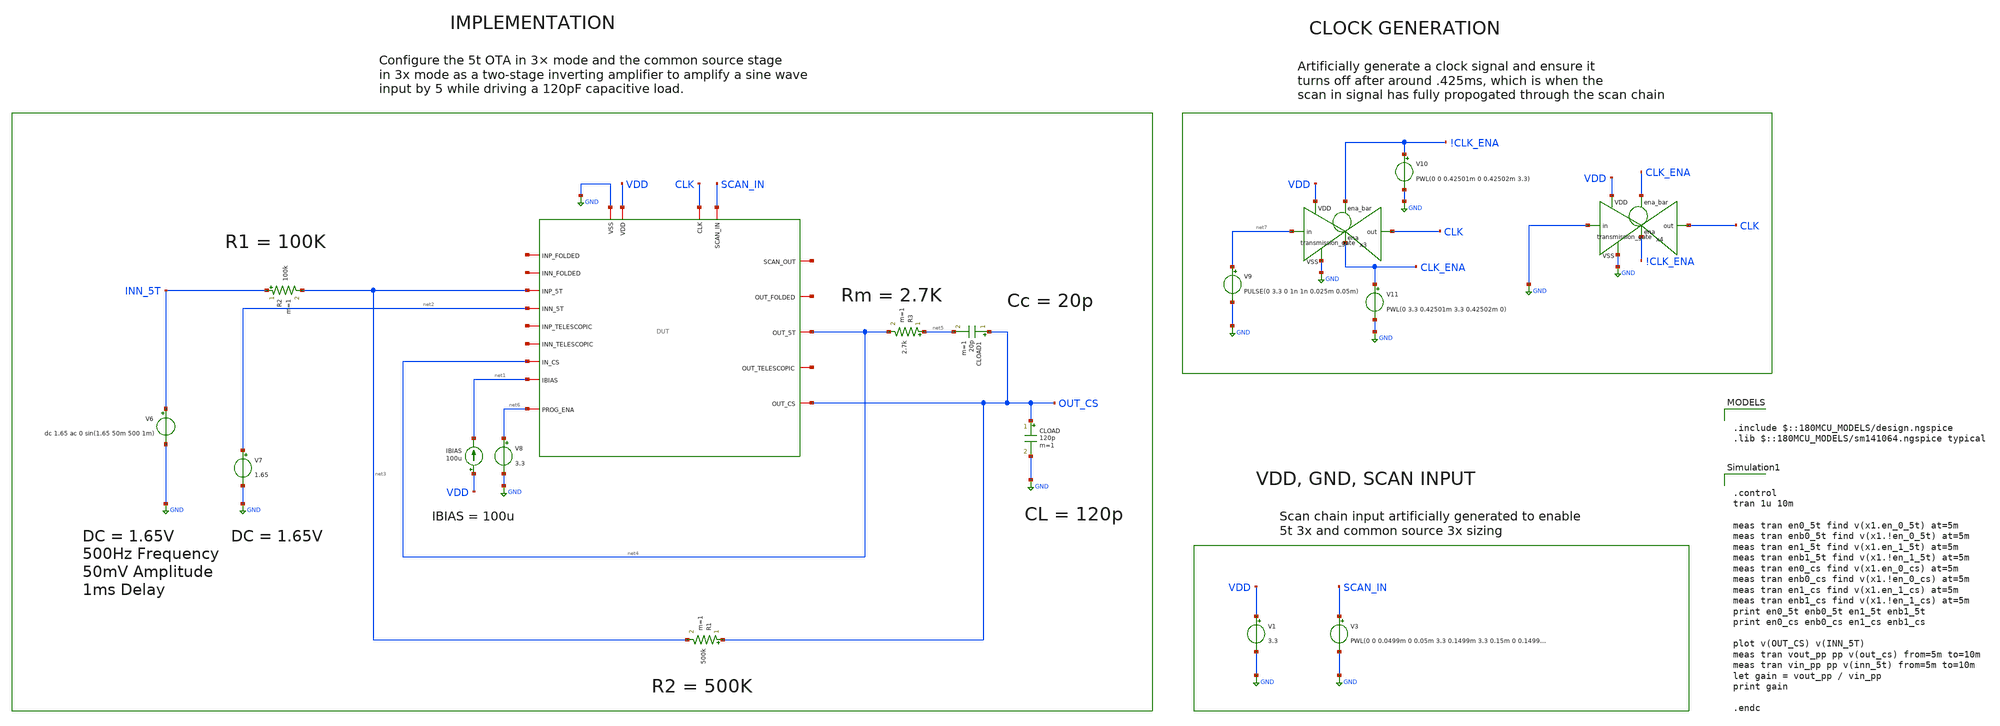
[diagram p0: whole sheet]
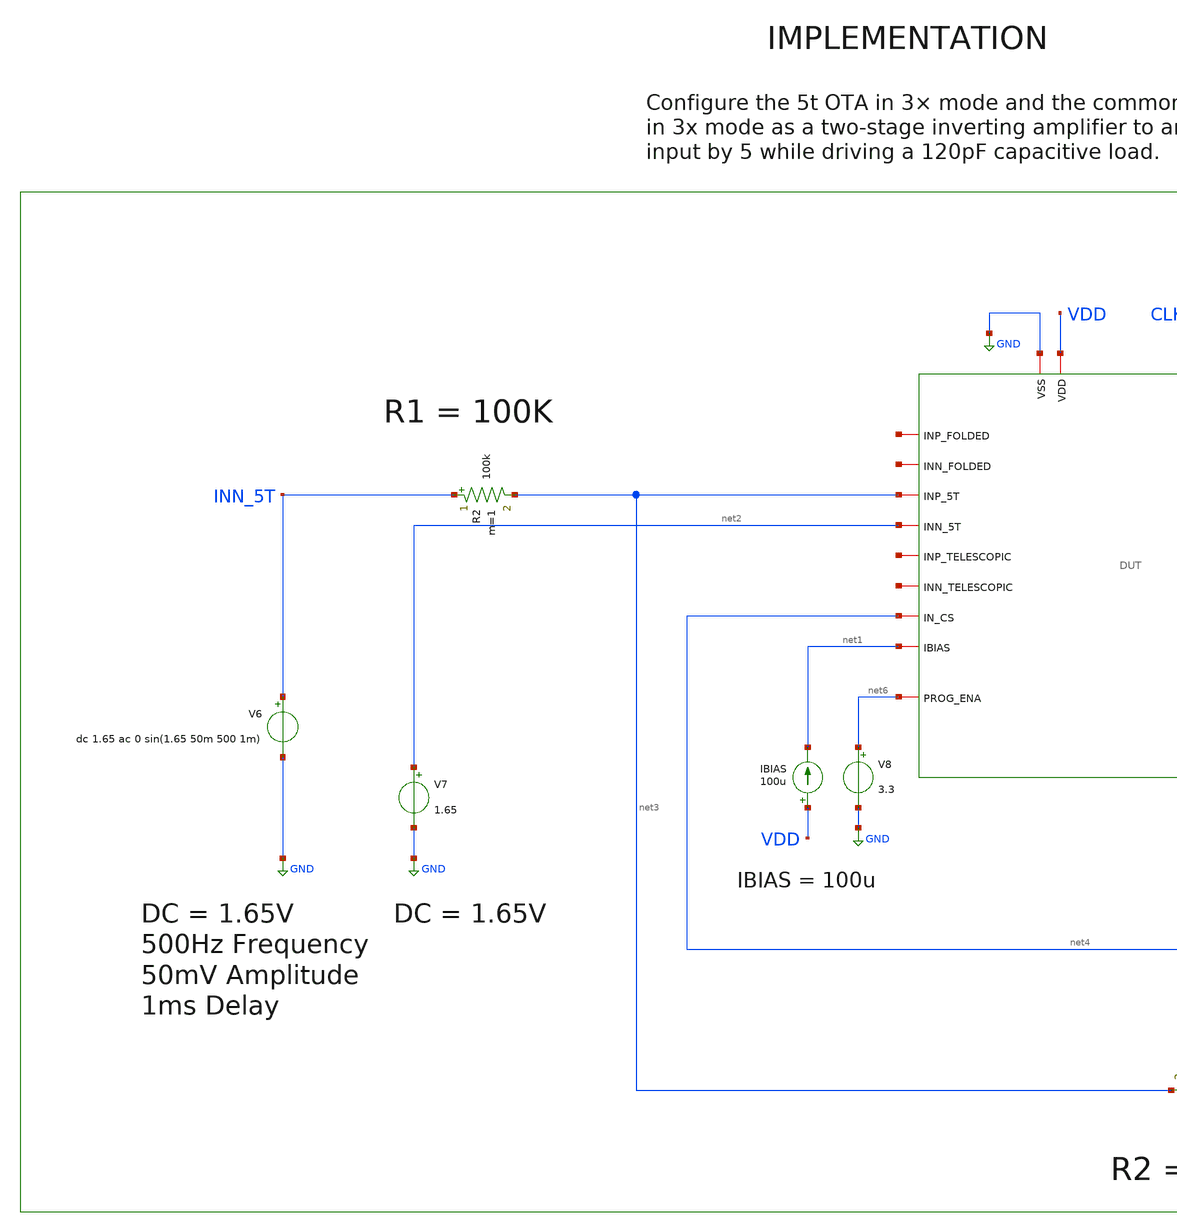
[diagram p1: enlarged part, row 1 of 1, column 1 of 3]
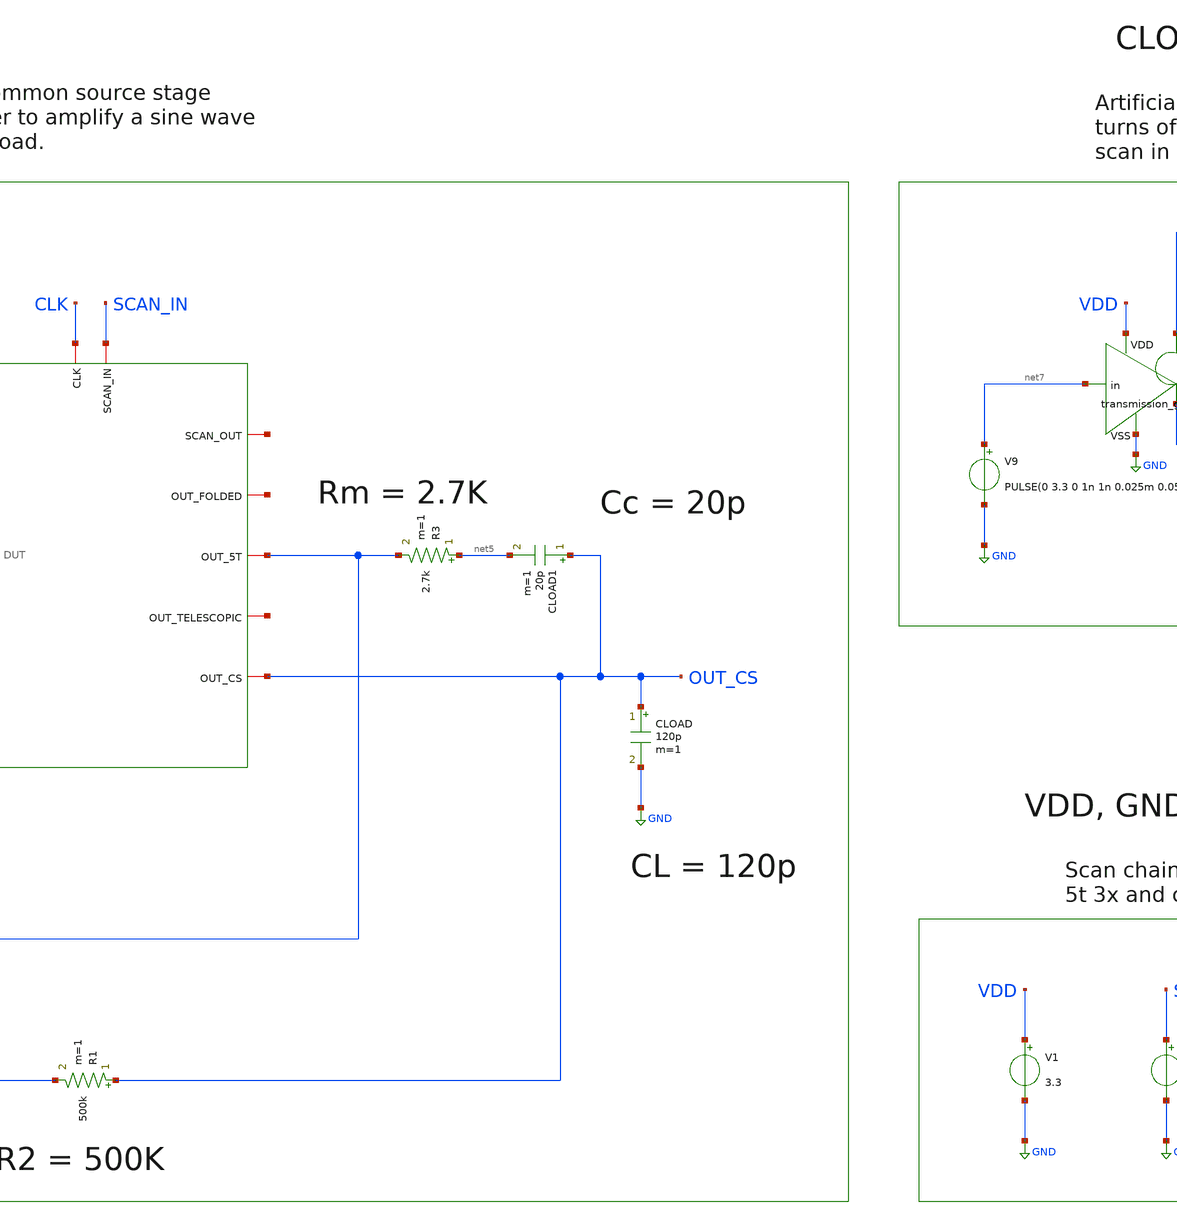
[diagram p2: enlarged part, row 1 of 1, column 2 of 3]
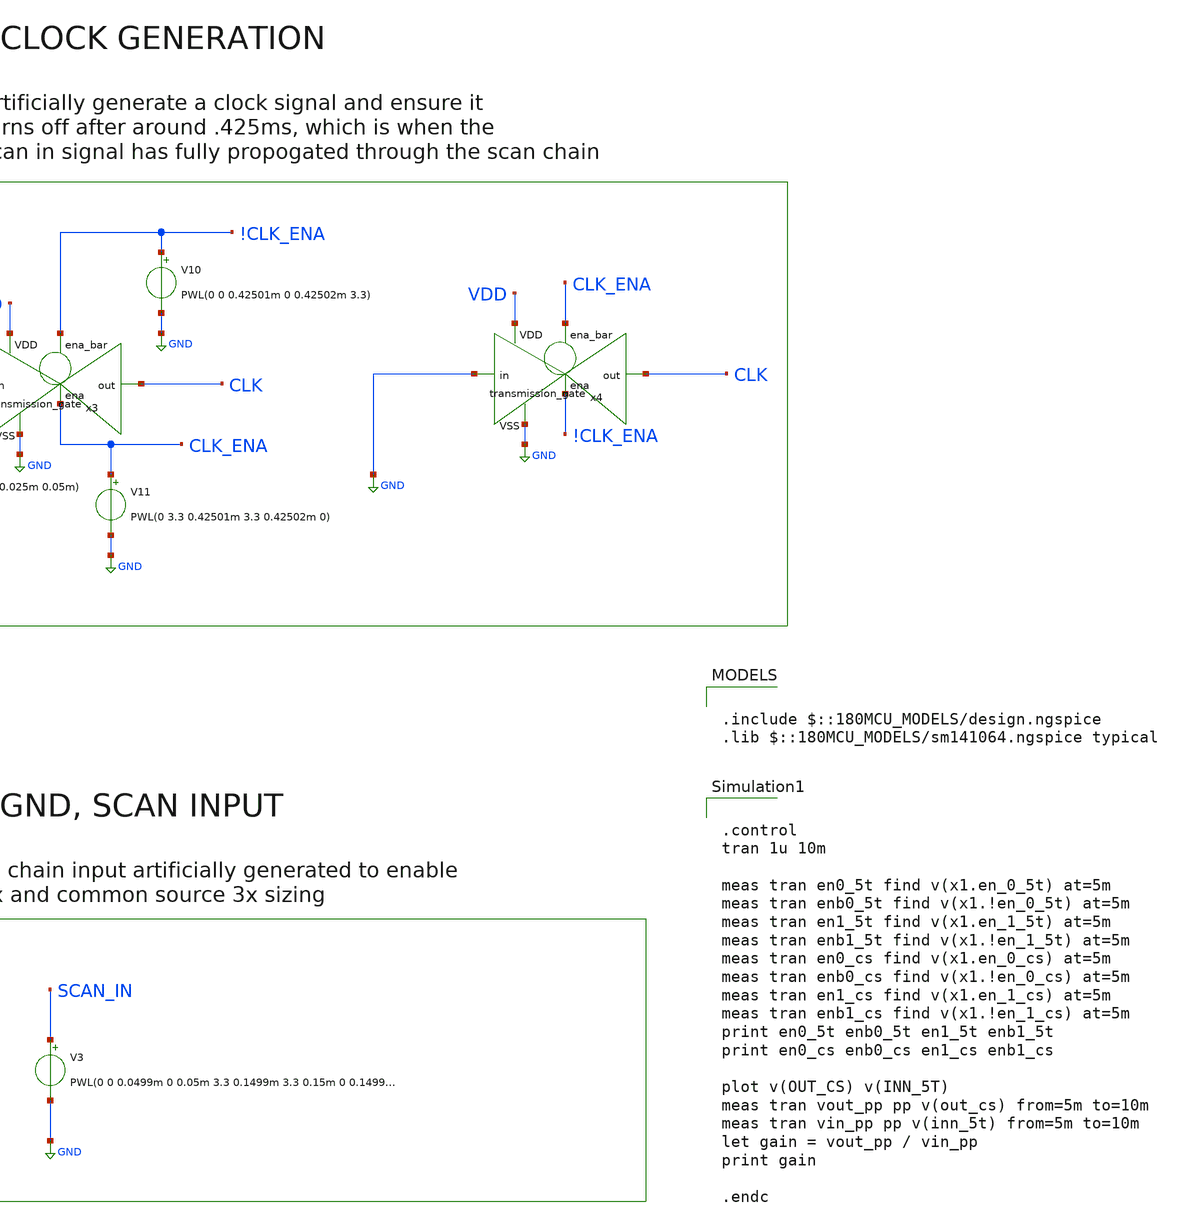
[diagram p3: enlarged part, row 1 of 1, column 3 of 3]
** sch_path: designs/libs/core_tb/sl/ota_5t/two_stage/5t_inverting_cs.sch
**.subckt 5t_inverting_cs
V3 SCAN_IN GND PWL(0 0 0.0499m 0 0.05m 3.3 0.1499m 3.3 0.15m 0 0.1499m 0 0.15m 3.3 0.24999m 3.3
+ 0.25m 0)
V1 VDD GND 3.3
IBIAS VDD net1 100u
CLOAD OUT_CS GND 120p m=1
R3 net5 net4 2.7k m=1
CLOAD1 OUT_CS net5 20p m=1
V7 net2 GND 1.65
R2 INN_5T net3 100k m=1
R1 OUT_CS net3 500k m=1
V6 INN_5T GND dc 1.65 ac 0 sin(1.65 50m 500 1m)
x1 CLK net8 SCAN_IN GND VDD net9 net10 net4 net1 net11 net3 net2 net12 net13 OUT_CS net4 net14 net6
+ DUT
V8 net6 GND 3.3
V9 net7 GND PULSE(0 3.3 0 1n 1n 0.025m 0.05m)
x3 !CLK_ENA VDD CLK net7 GND CLK_ENA transmission_gate
V10 !CLK_ENA GND PWL(0 0 0.42501m 0 0.42502m 3.3)
V11 CLK_ENA GND PWL(0 3.3 0.42501m 3.3 0.42502m 0)
x4 CLK_ENA VDD CLK GND GND !CLK_ENA transmission_gate
**** begin user architecture code

.include $::180MCU_MODELS/design.ngspice
.lib $::180MCU_MODELS/sm141064.ngspice typical



.control
tran 1u 10m

meas tran en0_5t find v(x1.en_0_5t) at=5m
meas tran enb0_5t find v(x1.!en_0_5t) at=5m
meas tran en1_5t find v(x1.en_1_5t) at=5m
meas tran enb1_5t find v(x1.!en_1_5t) at=5m
meas tran en0_cs find v(x1.en_0_cs) at=5m
meas tran enb0_cs find v(x1.!en_0_cs) at=5m
meas tran en1_cs find v(x1.en_1_cs) at=5m
meas tran enb1_cs find v(x1.!en_1_cs) at=5m
print en0_5t enb0_5t en1_5t enb1_5t
print en0_cs enb0_cs en1_cs enb1_cs

plot v(OUT_CS) v(INN_5T)
meas tran vout_pp pp v(out_cs) from=5m to=10m
meas tran vin_pp pp v(inn_5t) from=5m to=10m
let gain = vout_pp / vin_pp
print gain

.endc


**** end user architecture code
**.ends
.GLOBAL GND
.end
